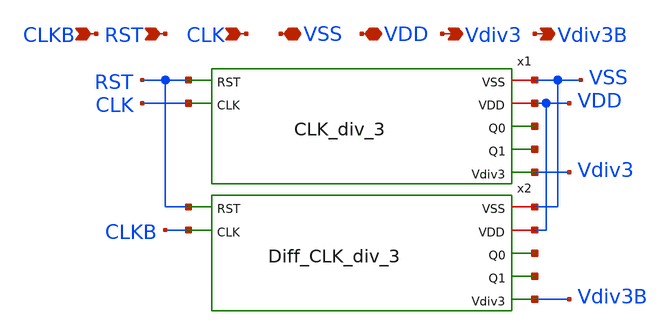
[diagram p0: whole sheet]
** sch_path: Clock_Generator_PAKISTAN_02/Schematics/DIFFER_CLK_div_3.sch
**.subckt DIFFER_CLK_div_3 CLK VSS VDD RST Vdiv3 Vdiv3B CLKB
*.ipin CLK
*.iopin VSS
*.iopin VDD
*.ipin RST
*.opin Vdiv3
*.opin Vdiv3B
*.ipin CLKB
x1 VSS VDD net1 net2 RST Vdiv3 CLK CLK_div_3
x2 VSS VDD net3 net4 RST Vdiv3B CLKB Diff_CLK_div_3
**.ends
.end
